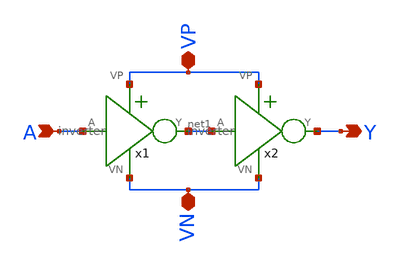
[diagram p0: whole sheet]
** sch_path: mp1/buffer/buffer.sch
**.subckt buffer VP VN A Y
*.iopin VP
*.iopin VN
*.ipin A
*.opin Y
x1 VP A net1 VN inverter
x2 VP net1 Y VN inverter
**.ends

* expanding   symbol:  /home/madvlsi/Documents/vlsi/mp1/inverter/inverter.sym # of pins=4
** sym_path: mp1/inverter/inverter.sym
** sch_path: mp1/inverter/inverter.sch
.subckt inverter VP A Y VN
*.iopin VP
*.iopin VN
*.ipin A
*.opin Y
XM1 Y A VN VN sky130_fd_pr__nfet_01v8 L=0.15 W=1 nf=1 ad='int((nf+1)/2) * W/nf * 0.29' as='int((nf+2)/2) * W/nf * 0.29'
+ pd='2*int((nf+1)/2) * (W/nf + 0.29)' ps='2*int((nf+2)/2) * (W/nf + 0.29)' nrd='0.29 / W' nrs='0.29 / W'
+ sa=0 sb=0 sd=0 mult=1 m=1
XM2 Y A VP VP sky130_fd_pr__pfet_01v8 L=0.15 W=1 nf=1 ad='int((nf+1)/2) * W/nf * 0.29' as='int((nf+2)/2) * W/nf * 0.29'
+ pd='2*int((nf+1)/2) * (W/nf + 0.29)' ps='2*int((nf+2)/2) * (W/nf + 0.29)' nrd='0.29 / W' nrs='0.29 / W'
+ sa=0 sb=0 sd=0 mult=1 m=1
.ends

.end
